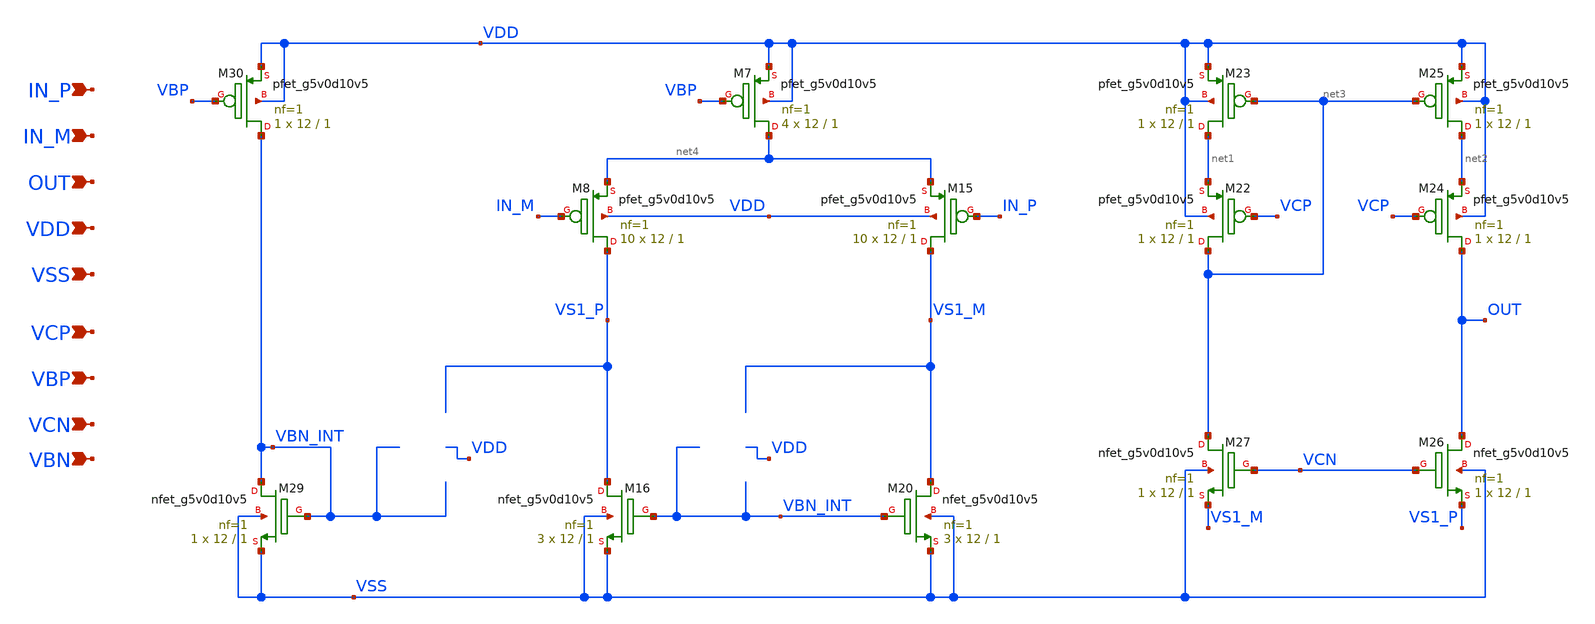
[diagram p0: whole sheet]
** sch_path: design/folded-cascode-p-in/folded_cascode_p_in.sch
**.subckt folded_cascode_p_in IN_P IN_M OUT VDD VSS VCP VBP VCN VBN
*.ipin IN_P
*.ipin IN_M
*.ipin OUT
*.ipin VDD
*.ipin VSS
*.ipin VCP
*.ipin VBP
*.ipin VCN
*.ipin VBN
XM7 net4 VBP VDD VDD sky130_fd_pr__pfet_g5v0d10v5 L=1 W=12 nf=1 ad='int((nf+1)/2) * W/nf * 0.29' as='int((nf+2)/2) * W/nf * 0.29'
+ pd='2*int((nf+1)/2) * (W/nf + 0.29)' ps='2*int((nf+2)/2) * (W/nf + 0.29)' nrd='0.29 / W' nrs='0.29 / W'
+ sa=0 sb=0 sd=0 mult=4 m=4
XM8 VS1_P IN_M net4 VDD sky130_fd_pr__pfet_g5v0d10v5 L=1 W=12 nf=1 ad='int((nf+1)/2) * W/nf * 0.29' as='int((nf+2)/2) * W/nf * 0.29'
+ pd='2*int((nf+1)/2) * (W/nf + 0.29)' ps='2*int((nf+2)/2) * (W/nf + 0.29)' nrd='0.29 / W' nrs='0.29 / W'
+ sa=0 sb=0 sd=0 mult=10 m=10
XM15 VS1_M IN_P net4 VDD sky130_fd_pr__pfet_g5v0d10v5 L=1 W=12 nf=1 ad='int((nf+1)/2) * W/nf * 0.29'
+ as='int((nf+2)/2) * W/nf * 0.29' pd='2*int((nf+1)/2) * (W/nf + 0.29)' ps='2*int((nf+2)/2) * (W/nf + 0.29)'
+ nrd='0.29 / W' nrs='0.29 / W' sa=0 sb=0 sd=0 mult=10 m=10
XM16 VS1_P VBN_INT VSS VSS sky130_fd_pr__nfet_g5v0d10v5 L=1 W=12 nf=1 ad='int((nf+1)/2) * W/nf * 0.29'
+ as='int((nf+2)/2) * W/nf * 0.29' pd='2*int((nf+1)/2) * (W/nf + 0.29)' ps='2*int((nf+2)/2) * (W/nf + 0.29)'
+ nrd='0.29 / W' nrs='0.29 / W' sa=0 sb=0 sd=0 mult=3 m=3
XM20 VS1_M VBN_INT VSS VSS sky130_fd_pr__nfet_g5v0d10v5 L=1 W=12 nf=1 ad='int((nf+1)/2) * W/nf * 0.29'
+ as='int((nf+2)/2) * W/nf * 0.29' pd='2*int((nf+1)/2) * (W/nf + 0.29)' ps='2*int((nf+2)/2) * (W/nf + 0.29)'
+ nrd='0.29 / W' nrs='0.29 / W' sa=0 sb=0 sd=0 mult=3 m=3
XM22 net3 VCP net1 VDD sky130_fd_pr__pfet_g5v0d10v5 L=1 W=12 nf=1 ad='int((nf+1)/2) * W/nf * 0.29' as='int((nf+2)/2) * W/nf * 0.29'
+ pd='2*int((nf+1)/2) * (W/nf + 0.29)' ps='2*int((nf+2)/2) * (W/nf + 0.29)' nrd='0.29 / W' nrs='0.29 / W'
+ sa=0 sb=0 sd=0 mult=1 m=1
XM23 net1 net3 VDD VDD sky130_fd_pr__pfet_g5v0d10v5 L=1 W=12 nf=1 ad='int((nf+1)/2) * W/nf * 0.29' as='int((nf+2)/2) * W/nf * 0.29'
+ pd='2*int((nf+1)/2) * (W/nf + 0.29)' ps='2*int((nf+2)/2) * (W/nf + 0.29)' nrd='0.29 / W' nrs='0.29 / W'
+ sa=0 sb=0 sd=0 mult=1 m=1
XM24 OUT VCP net2 VDD sky130_fd_pr__pfet_g5v0d10v5 L=1 W=12 nf=1 ad='int((nf+1)/2) * W/nf * 0.29' as='int((nf+2)/2) * W/nf * 0.29'
+ pd='2*int((nf+1)/2) * (W/nf + 0.29)' ps='2*int((nf+2)/2) * (W/nf + 0.29)' nrd='0.29 / W' nrs='0.29 / W'
+ sa=0 sb=0 sd=0 mult=1 m=1
XM25 net2 net3 VDD VDD sky130_fd_pr__pfet_g5v0d10v5 L=1 W=12 nf=1 ad='int((nf+1)/2) * W/nf * 0.29' as='int((nf+2)/2) * W/nf * 0.29'
+ pd='2*int((nf+1)/2) * (W/nf + 0.29)' ps='2*int((nf+2)/2) * (W/nf + 0.29)' nrd='0.29 / W' nrs='0.29 / W'
+ sa=0 sb=0 sd=0 mult=1 m=1
XM26 OUT VCN VS1_P VSS sky130_fd_pr__nfet_g5v0d10v5 L=1 W=12 nf=1 ad='int((nf+1)/2) * W/nf * 0.29' as='int((nf+2)/2) * W/nf * 0.29'
+ pd='2*int((nf+1)/2) * (W/nf + 0.29)' ps='2*int((nf+2)/2) * (W/nf + 0.29)' nrd='0.29 / W' nrs='0.29 / W'
+ sa=0 sb=0 sd=0 mult=1 m=1
XM27 net3 VCN VS1_M VSS sky130_fd_pr__nfet_g5v0d10v5 L=1 W=12 nf=1 ad='int((nf+1)/2) * W/nf * 0.29' as='int((nf+2)/2) * W/nf * 0.29'
+ pd='2*int((nf+1)/2) * (W/nf + 0.29)' ps='2*int((nf+2)/2) * (W/nf + 0.29)' nrd='0.29 / W' nrs='0.29 / W'
+ sa=0 sb=0 sd=0 mult=1 m=1
XM29 VBN_INT VBN_INT VSS VSS sky130_fd_pr__nfet_g5v0d10v5 L=1 W=12 nf=1 ad='int((nf+1)/2) * W/nf * 0.29'
+ as='int((nf+2)/2) * W/nf * 0.29' pd='2*int((nf+1)/2) * (W/nf + 0.29)' ps='2*int((nf+2)/2) * (W/nf + 0.29)'
+ nrd='0.29 / W' nrs='0.29 / W' sa=0 sb=0 sd=0 mult=1 m=1
XM30 VBN_INT VBP VDD VDD sky130_fd_pr__pfet_g5v0d10v5 L=1 W=12 nf=1 ad='int((nf+1)/2) * W/nf * 0.29'
+ as='int((nf+2)/2) * W/nf * 0.29' pd='2*int((nf+1)/2) * (W/nf + 0.29)' ps='2*int((nf+2)/2) * (W/nf + 0.29)'
+ nrd='0.29 / W' nrs='0.29 / W' sa=0 sb=0 sd=0 mult=1 m=1
**.ends
.end
